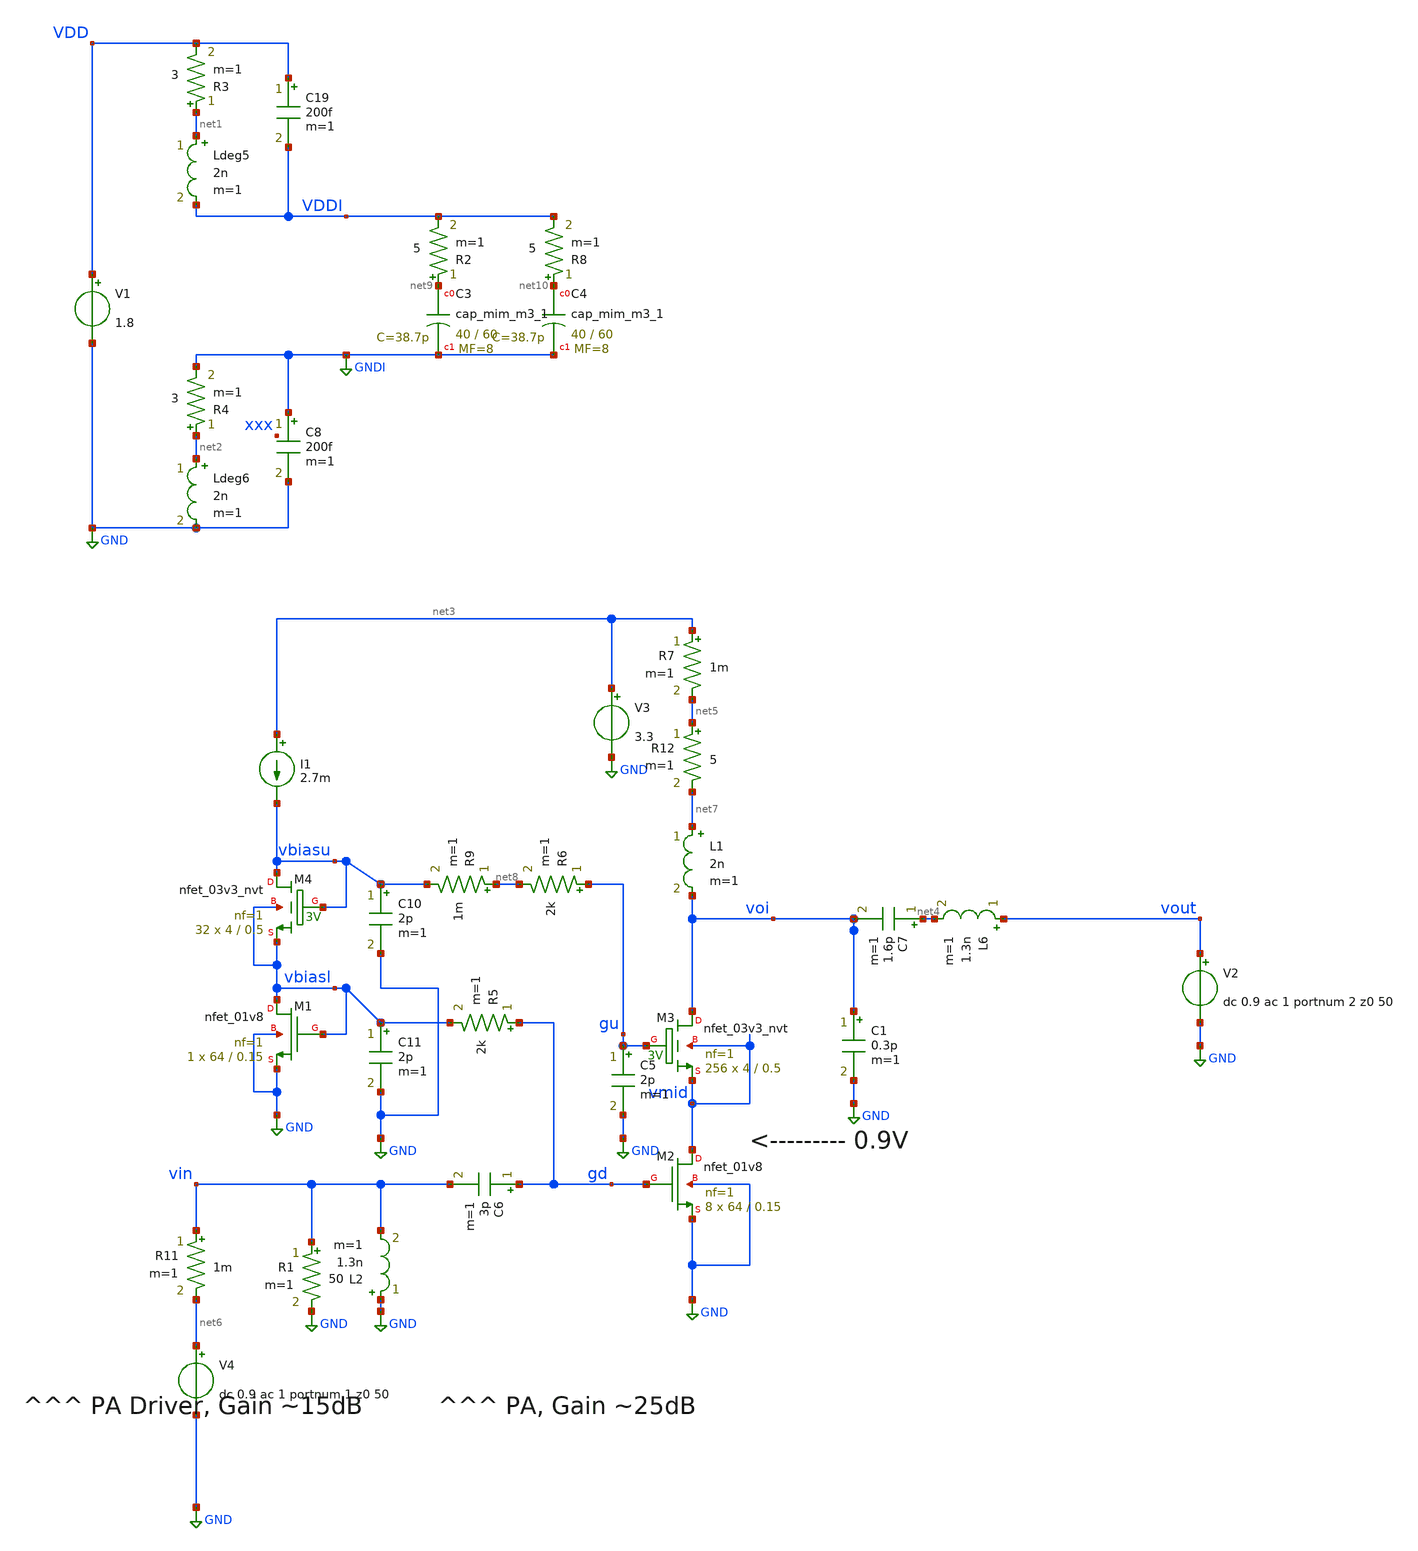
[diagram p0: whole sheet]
** sch_path: xschem/2stack_res_matching_newbias.sch
**.subckt 2stack_res_matching_newbias
V1 VDD GND 1.8
Ldeg5 net1 VDDI 2n m=1
R3 net1 VDD 3 m=1
Ldeg6 net2 GND 2n m=1
R4 net2 GNDI 3 m=1
XC3 net9 GNDI sky130_fd_pr__cap_mim_m3_1 W=40 L=60 MF=8 m=8
C8 GNDI GND 200f m=1
C19 VDD VDDI 200f m=1
R2 net9 VDDI 5 m=1
XC4 net10 GNDI sky130_fd_pr__cap_mim_m3_1 W=40 L=60 MF=8 m=8
R8 net10 VDDI 5 m=1
V3 net3 GND 3.3
L1 net7 voi 2n m=1
L6 vout net4 1.3n m=1
C7 net4 voi 1.6p m=1
C1 voi GND 0.3p m=1
R5 gd vbiasl 2k m=1
XM3 voi gu vmid vmid sky130_fd_pr__nfet_03v3_nvt L=0.5 W=4 nf=1 ad='int((nf+1)/2) * W/nf * 0.29' as='int((nf+2)/2) * W/nf * 0.29'
+ pd='2*int((nf+1)/2) * (W/nf + 0.29)' ps='2*int((nf+2)/2) * (W/nf + 0.29)' nrd='0.29 / W' nrs='0.29 / W'
+ sa=0 sb=0 sd=0 mult=256 m=256
R6 gu net8 2k m=1
C5 gu GND 2p m=1
R7 net3 net5 1m m=1
XM2 vmid gd GND GND sky130_fd_pr__nfet_01v8 L=0.15 W=64 nf=1 ad='int((nf+1)/2) * W/nf * 0.29' as='int((nf+2)/2) * W/nf * 0.29'
+ pd='2*int((nf+1)/2) * (W/nf + 0.29)' ps='2*int((nf+2)/2) * (W/nf + 0.29)' nrd='0.29 / W' nrs='0.29 / W'
+ sa=0 sb=0 sd=0 mult=8 m=8
R11 vin net6 1m m=1
R12 net5 net7 5 m=1
C6 gd vin 3p m=1
XM1 vbiasl vbiasl GND GND sky130_fd_pr__nfet_01v8 L=0.15 W=64 nf=1 ad='int((nf+1)/2) * W/nf * 0.29' as='int((nf+2)/2) * W/nf * 0.29'
+ pd='2*int((nf+1)/2) * (W/nf + 0.29)' ps='2*int((nf+2)/2) * (W/nf + 0.29)' nrd='0.29 / W' nrs='0.29 / W'
+ sa=0 sb=0 sd=0 mult=1 m=1
XM4 vbiasu vbiasu vbiasl vbiasl sky130_fd_pr__nfet_03v3_nvt L=0.5 W=4 nf=1 ad='int((nf+1)/2) * W/nf * 0.29'
+ as='int((nf+2)/2) * W/nf * 0.29' pd='2*int((nf+1)/2) * (W/nf + 0.29)' ps='2*int((nf+2)/2) * (W/nf + 0.29)'
+ nrd='0.29 / W' nrs='0.29 / W' sa=0 sb=0 sd=0 mult=32 m=32
I1 net3 vbiasu 2.7m
C10 vbiasu GND 2p m=1
C11 vbiasl GND 2p m=1
R9 net8 vbiasu 1m m=1
R1 vin GND 50 m=1
V4 net6 GND dc 0.9 ac 1 portnum 1 z0 50
V2 vout GND dc 0.9 ac 1 portnum 2 z0 50
L2 GND vin 1.3n m=1
**** begin user architecture code
.lib $::SKYWATER_MODELS/sky130.lib.spice tt
* .include $::PDKPATH/libs.ref/sky130_fd_sc_hvl/spice/sky130_fd_sc_hvl.spice



.options savecurrents
* XMU_0 gu voi mid mid rf_nfet_6xaM02_extracted
* XMU_1 gu voi mid mid rf_nfet_6xaM02_extracted
* XMU_2 gu voi mid mid rf_nfet_6xaM02_extracted
* XMU_3 gu voi mid mid rf_nfet_6xaM02_extracted
* XMU_4 gu voi mid mid rf_nfet_6xaM02_extracted
* XMU_5 gu voi mid mid rf_nfet_6xaM02_extracted
* XMD_0 gd mid gnd gnd rf_nfet_6xaM02_extracted
* XMD_1 gd mid gnd gnd rf_nfet_6xaM02_extracted
* XMD_2 gd mid gnd gnd rf_nfet_6xaM02_extracted
* XMD_3 gd mid gnd gnd rf_nfet_6xaM02_extracted
* XMD_4 gd mid gnd gnd rf_nfet_6xaM02_extracted
* XMD_5 gd mid gnd gnd rf_nfet_6xaM02_extracted
* .tran 5ps 20ns
.sp dec 1000 1e9 10e9 1
.control
run
display
plot @r5[i]
let zout=@rload[r]
let zin=50
* meas TRAN vout_rms rms v(vout)
* meas TRAN isp_hi_avg  avg @r7[i]
* meas TRAN isp_mid_avg avg @r9[i]
* meas TRAN vin_rms rms v(vin)
* meas TRAN isp_1p8_avg avg @rsense2[i]
* let psp_rms  = isp_hi_avg*3.6 + isp_mid_avg*2.2
* let pout_rms = vout_rms^2/zout
* let pin_rms  = vin_rms^2/zin
* print psp_rms
* print ((pout_rms-pin_rms)/psp_rms)*100
* print 10*log10(pout_rms*1000)

* plot gd vmid voi vout

* let pout = mag(@rload[i]*vout)
* let poutdbm = log10((pout/(1e-3))*10
* plot pout

.endc


**** end user architecture code
**.ends
.GLOBAL GND
.GLOBAL GNDI
.end
